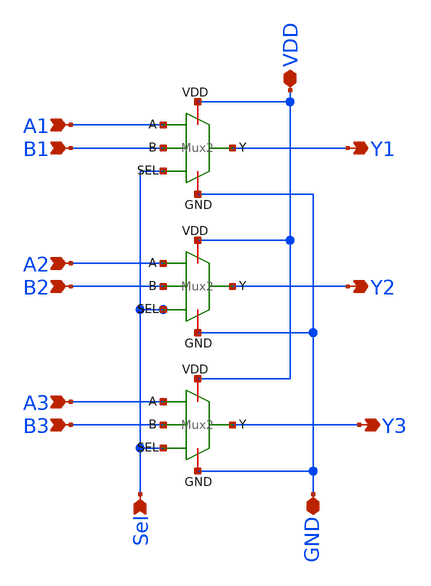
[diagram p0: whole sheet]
** sch_path: Mux2In-3BusW.sch
**.subckt Mux2In-3BusW A1 B1 A2 B2 A3 B3 Y1 Y2 Y3 Sel GND VDD
*.ipin A1
*.ipin B1
*.ipin A2
*.ipin B2
*.ipin A3
*.ipin B3
*.opin Y1
*.opin Y2
*.opin Y3
*.ipin Sel
*.iopin GND
*.iopin VDD
x10 VDD A1 GND Y1 B1 Sel Mux2
x11 VDD A2 GND Y2 B2 Sel Mux2
x12 VDD A3 GND Y3 B3 Sel Mux2
**.ends
.end
